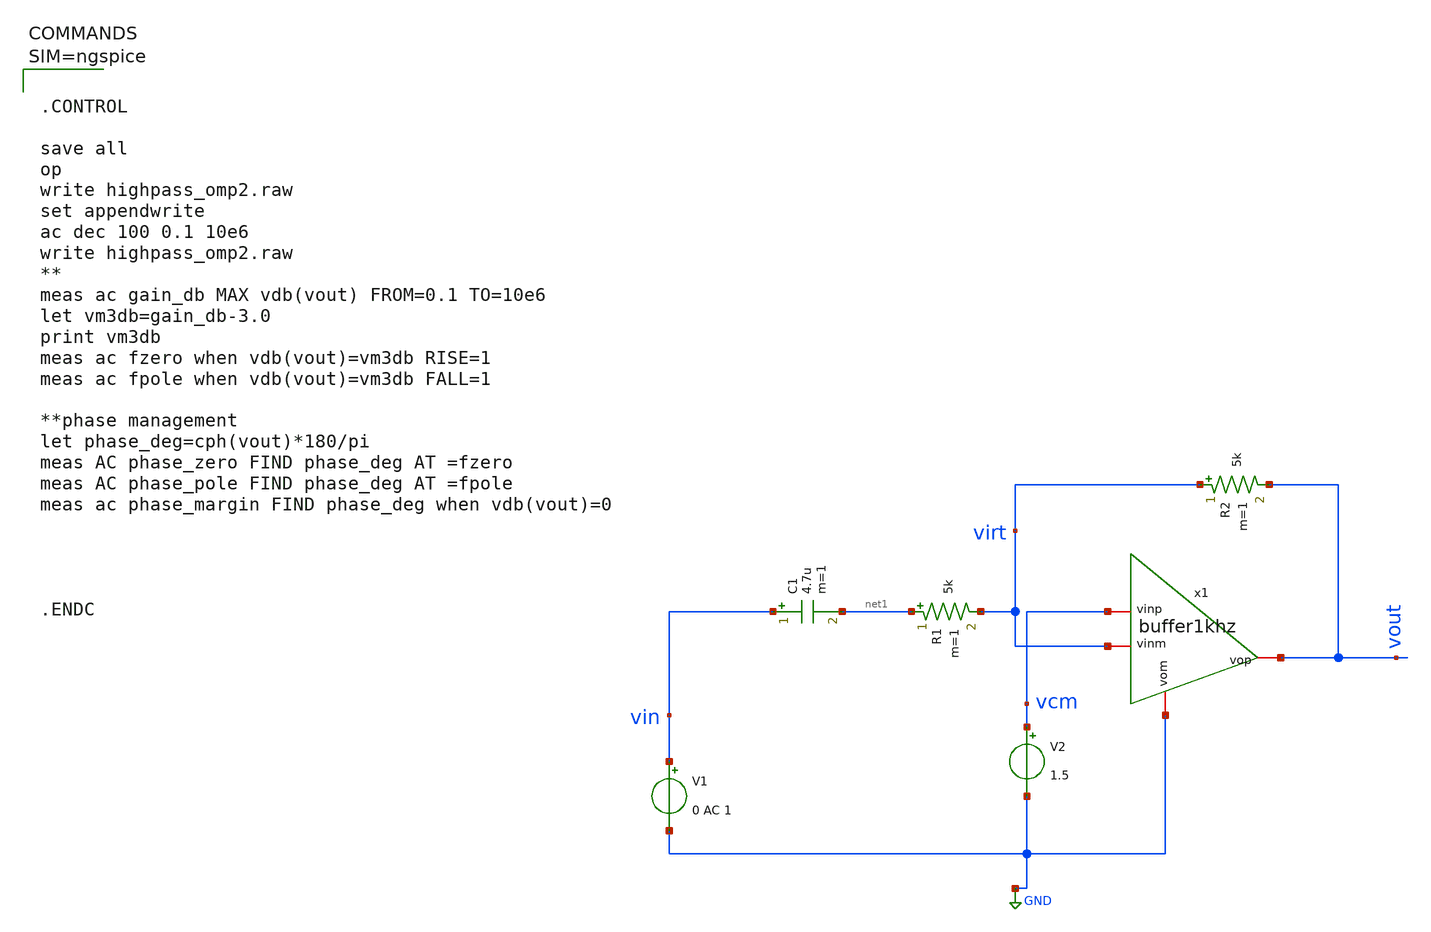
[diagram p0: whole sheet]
** sch_path: work/xschem/highpass_omp2.sch
**.subckt highpass_omp2
x1 vout vcm GND virt buffer1khz
R1 net1 virt 5k m=1
C1 vin net1 4.7u m=1
R2 virt vout 5k m=1
V1 vin GND 0 AC 1
V2 vcm GND 1.5
**** begin user architecture code



.CONTROL

save all
op
write highpass_omp2.raw
set appendwrite
ac dec 100 0.1 10e6
write highpass_omp2.raw
**
meas ac gain_db MAX vdb(vout) FROM=0.1 TO=10e6
let vm3db=gain_db-3.0
print vm3db
meas ac fzero when vdb(vout)=vm3db RISE=1
meas ac fpole when vdb(vout)=vm3db FALL=1

**phase management
let phase_deg=cph(vout)*180/pi
meas AC phase_zero FIND phase_deg AT =fzero
meas AC phase_pole FIND phase_deg AT =fpole
meas ac phase_margin FIND phase_deg when vdb(vout)=0




.ENDC



**** end user architecture code
**.ends

* expanding   symbol:  buffer1khz.sym # of pins=4
** sym_path: work/xschem/buffer1khz.sym
** sch_path: work/xschem/buffer1khz.sch
.subckt buffer1khz vop vinp vom vinm
*.iopin vop
*.iopin vom
*.iopin vinp
*.iopin vinm
R1 net1 net2 15.9k m=1
C1 net2 GND 10n m=1
E1 net1 GND vinp vinm 1000
E2 vop vom net2 GND 1
**** begin user architecture code



.CONTROL

save all
set appendfile
wrtie buffer1khz.raw

.ENDC



**** end user architecture code
.ends

.GLOBAL GND
.end
